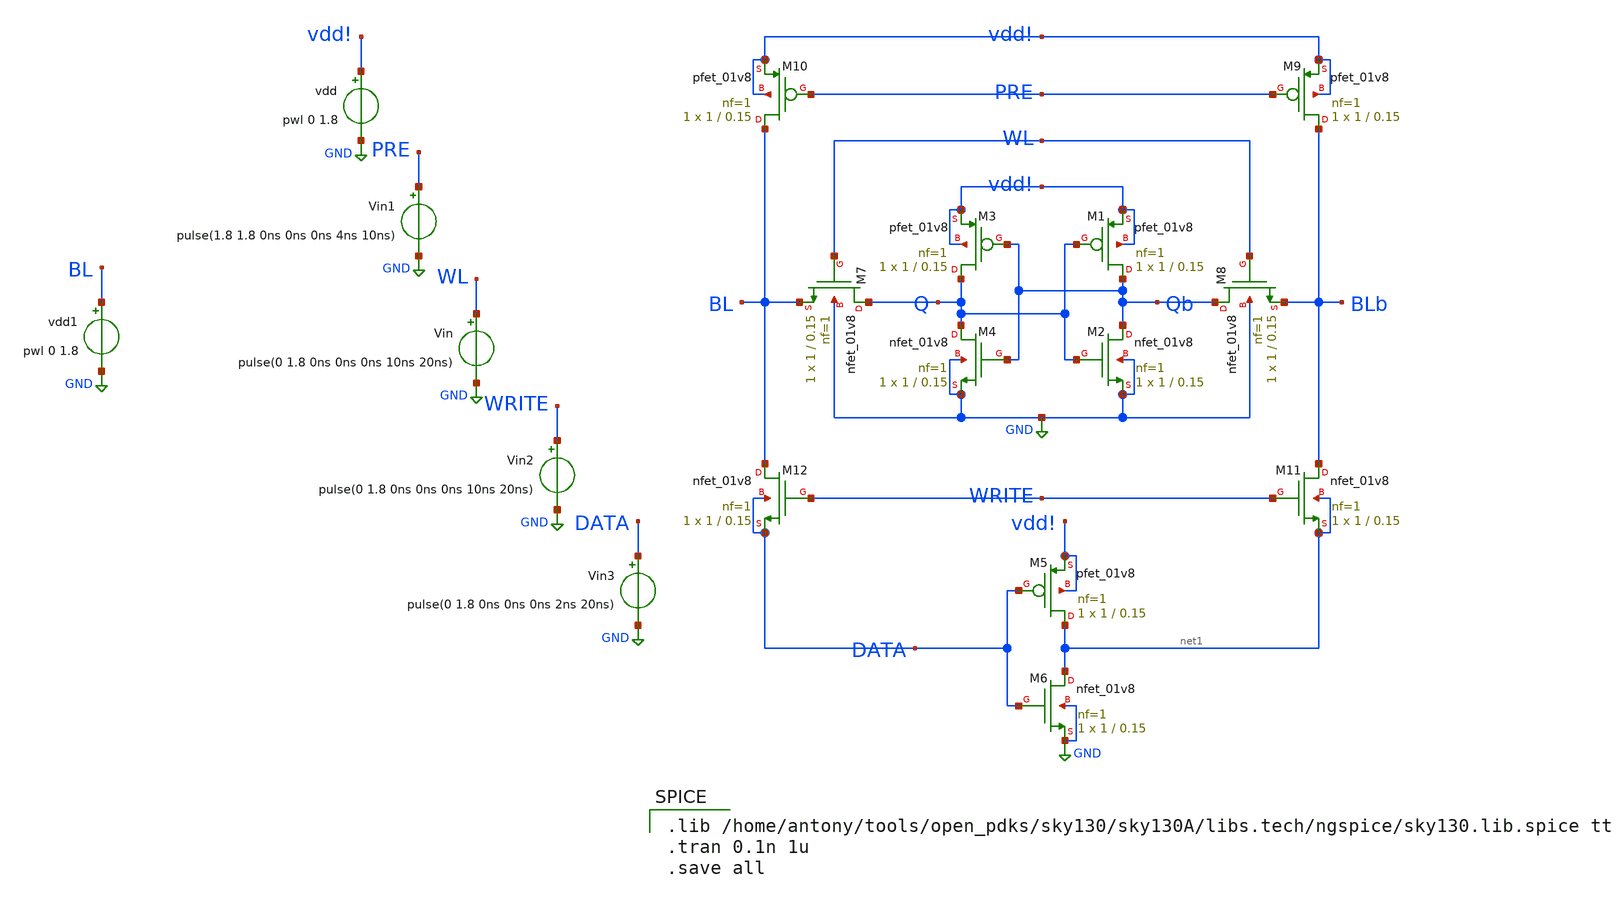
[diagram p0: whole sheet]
** sch_path: 6t_sram_130_testbench.sch
**.subckt 6t_sram_130_testbench
Vin WL GND pulse(0 1.8 0ns 0ns 0ns 10ns 20ns)
XM1 Qb Q vdd! vdd! sky130_fd_pr__pfet_01v8 L=0.15 W=1 nf=1 ad='int((nf+1)/2) * W/nf * 0.29' as='int((nf+2)/2) * W/nf * 0.29'
+ pd='2*int((nf+1)/2) * (W/nf + 0.29)' ps='2*int((nf+2)/2) * (W/nf + 0.29)' nrd='0.29 / W' nrs='0.29 / W'
+ sa=0 sb=0 sd=0 mult=1 m=1
XM2 Qb Q GND GND sky130_fd_pr__nfet_01v8 L=0.15 W=1 nf=1 ad='int((nf+1)/2) * W/nf * 0.29' as='int((nf+2)/2) * W/nf * 0.29'
+ pd='2*int((nf+1)/2) * (W/nf + 0.29)' ps='2*int((nf+2)/2) * (W/nf + 0.29)' nrd='0.29 / W' nrs='0.29 / W'
+ sa=0 sb=0 sd=0 mult=1 m=1
XM3 Q Qb vdd! vdd! sky130_fd_pr__pfet_01v8 L=0.15 W=1 nf=1 ad='int((nf+1)/2) * W/nf * 0.29' as='int((nf+2)/2) * W/nf * 0.29'
+ pd='2*int((nf+1)/2) * (W/nf + 0.29)' ps='2*int((nf+2)/2) * (W/nf + 0.29)' nrd='0.29 / W' nrs='0.29 / W'
+ sa=0 sb=0 sd=0 mult=1 m=1
XM4 Q Qb GND GND sky130_fd_pr__nfet_01v8 L=0.15 W=1 nf=1 ad='int((nf+1)/2) * W/nf * 0.29' as='int((nf+2)/2) * W/nf * 0.29'
+ pd='2*int((nf+1)/2) * (W/nf + 0.29)' ps='2*int((nf+2)/2) * (W/nf + 0.29)' nrd='0.29 / W' nrs='0.29 / W'
+ sa=0 sb=0 sd=0 mult=1 m=1
XM5 net1 DATA vdd! vdd! sky130_fd_pr__pfet_01v8 L=0.15 W=1 nf=1 ad='int((nf+1)/2) * W/nf * 0.29' as='int((nf+2)/2) * W/nf * 0.29'
+ pd='2*int((nf+1)/2) * (W/nf + 0.29)' ps='2*int((nf+2)/2) * (W/nf + 0.29)' nrd='0.29 / W' nrs='0.29 / W'
+ sa=0 sb=0 sd=0 mult=1 m=1
XM6 net1 DATA GND GND sky130_fd_pr__nfet_01v8 L=0.15 W=1 nf=1 ad='int((nf+1)/2) * W/nf * 0.29' as='int((nf+2)/2) * W/nf * 0.29'
+ pd='2*int((nf+1)/2) * (W/nf + 0.29)' ps='2*int((nf+2)/2) * (W/nf + 0.29)' nrd='0.29 / W' nrs='0.29 / W'
+ sa=0 sb=0 sd=0 mult=1 m=1
XM7 Q WL BL GND sky130_fd_pr__nfet_01v8 L=0.15 W=1 nf=1 ad='int((nf+1)/2) * W/nf * 0.29' as='int((nf+2)/2) * W/nf * 0.29'
+ pd='2*int((nf+1)/2) * (W/nf + 0.29)' ps='2*int((nf+2)/2) * (W/nf + 0.29)' nrd='0.29 / W' nrs='0.29 / W'
+ sa=0 sb=0 sd=0 mult=1 m=1
XM8 Qb WL BLb GND sky130_fd_pr__nfet_01v8 L=0.15 W=1 nf=1 ad='int((nf+1)/2) * W/nf * 0.29' as='int((nf+2)/2) * W/nf * 0.29'
+ pd='2*int((nf+1)/2) * (W/nf + 0.29)' ps='2*int((nf+2)/2) * (W/nf + 0.29)' nrd='0.29 / W' nrs='0.29 / W'
+ sa=0 sb=0 sd=0 mult=1 m=1
vdd vdd! GND pwl 0 1.8
XM9 BLb PRE vdd! vdd! sky130_fd_pr__pfet_01v8 L=0.15 W=1 nf=1 ad='int((nf+1)/2) * W/nf * 0.29' as='int((nf+2)/2) * W/nf * 0.29'
+ pd='2*int((nf+1)/2) * (W/nf + 0.29)' ps='2*int((nf+2)/2) * (W/nf + 0.29)' nrd='0.29 / W' nrs='0.29 / W'
+ sa=0 sb=0 sd=0 mult=1 m=1
XM10 BL PRE vdd! vdd! sky130_fd_pr__pfet_01v8 L=0.15 W=1 nf=1 ad='int((nf+1)/2) * W/nf * 0.29' as='int((nf+2)/2) * W/nf * 0.29'
+ pd='2*int((nf+1)/2) * (W/nf + 0.29)' ps='2*int((nf+2)/2) * (W/nf + 0.29)' nrd='0.29 / W' nrs='0.29 / W'
+ sa=0 sb=0 sd=0 mult=1 m=1
XM11 BLb WRITE net1 net1 sky130_fd_pr__nfet_01v8 L=0.15 W=1 nf=1 ad='int((nf+1)/2) * W/nf * 0.29' as='int((nf+2)/2) * W/nf * 0.29'
+ pd='2*int((nf+1)/2) * (W/nf + 0.29)' ps='2*int((nf+2)/2) * (W/nf + 0.29)' nrd='0.29 / W' nrs='0.29 / W'
+ sa=0 sb=0 sd=0 mult=1 m=1
XM12 BL WRITE DATA DATA sky130_fd_pr__nfet_01v8 L=0.15 W=1 nf=1 ad='int((nf+1)/2) * W/nf * 0.29' as='int((nf+2)/2) * W/nf * 0.29'
+ pd='2*int((nf+1)/2) * (W/nf + 0.29)' ps='2*int((nf+2)/2) * (W/nf + 0.29)' nrd='0.29 / W' nrs='0.29 / W'
+ sa=0 sb=0 sd=0 mult=1 m=1
Vin1 PRE GND pulse(1.8 1.8 0ns 0ns 0ns 4ns 10ns)
Vin2 WRITE GND pulse(0 1.8 0ns 0ns 0ns 10ns 20ns)
Vin3 DATA GND pulse(0 1.8 0ns 0ns 0ns 2ns 20ns)
vdd1 BL GND pwl 0 1.8
**** begin user architecture code

.lib /home/antony/tools/open_pdks/sky130/sky130A/libs.tech/ngspice/sky130.lib.spice tt
.tran 0.1n 1u
.save all

**** end user architecture code
**.ends
.GLOBAL GND
.end
